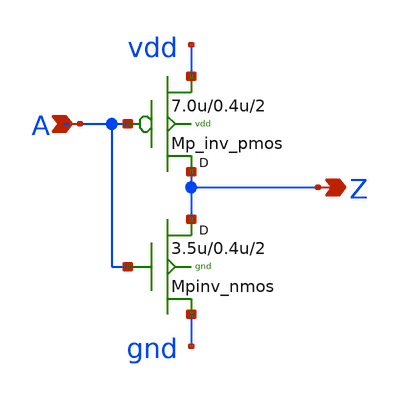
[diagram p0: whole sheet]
** sch_path: sram_2_64_scn4m_lcc/pinv_9.sch
**.subckt pinv_9 A Z
*.ipin A
*.opin Z
Mpinv_nmos Z A gnd gnd n w=3.5u l=0.4u m=2
Mp_inv_pmos Z A vdd vdd p w=7.0u l=0.4u m=2
**.ends
.end
